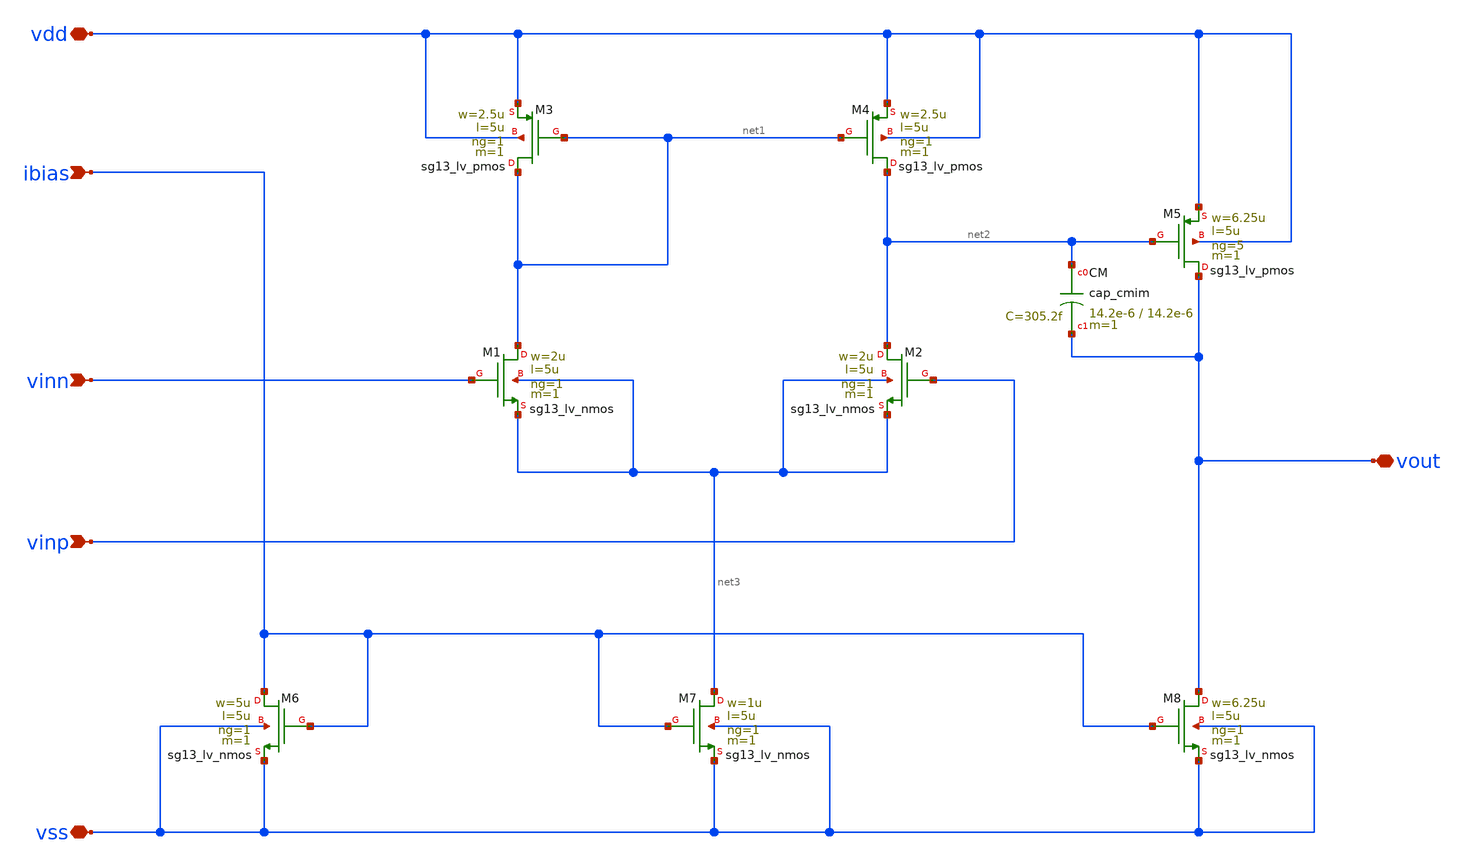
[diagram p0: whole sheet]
** sch_path: Testbench/ota-2stage.sch
**.subckt ota-2stage vdd vss ibias vout vinn vinp
*.iopin vdd
*.iopin vss
*.ipin ibias
*.iopin vout
*.ipin vinn
*.ipin vinp
XM1 net1 vinn net3 net3 sg13_lv_nmos w=2u l=5u ng=1 m=1 mm_ok=1
XM2 net2 vinp net3 net3 sg13_lv_nmos w=2u l=5u ng=1 m=1 mm_ok=1
XM4 net2 net1 vdd vdd sg13_lv_pmos w=2.5u l=5u ng=1 m=1 mm_ok=1
XM3 net1 net1 vdd vdd sg13_lv_pmos w=2.5u l=5u ng=1 m=1 mm_ok=1
XM5 vout net2 vdd vdd sg13_lv_pmos w=6.25u l=5u ng=5 m=1 mm_ok=1
XM6 ibias ibias vss vss sg13_lv_nmos w=5u l=5u ng=1 m=1 mm_ok=1
XM7 net3 ibias vss vss sg13_lv_nmos w=1u l=5u ng=1 m=1 mm_ok=1
XM8 vout ibias vss vss sg13_lv_nmos w=6.25u l=5u ng=1 m=1 mm_ok=1
XCM net2 vout cap_cmim w=14.2e-6 l=14.2e-6 m=1 mm_ok=1
**.ends
.end
